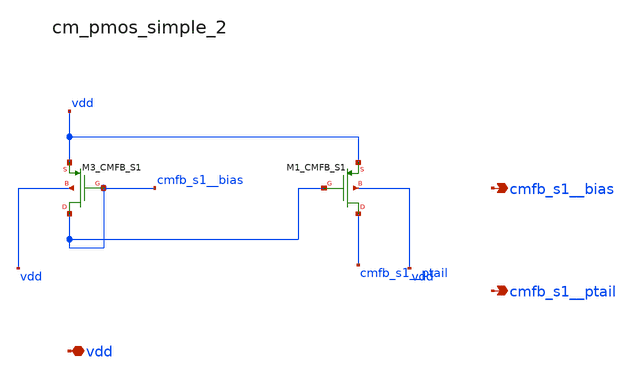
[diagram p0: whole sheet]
** sch_path: analog-db/raw/amp_035_fan_chopper_cmfb_dual/hier/blocks/cm_pmos_simple_2.sch
**.subckt cm_pmos_simple_2 vdd cmfb_s1__bias cmfb_s1__ptail
*.iopin vdd
*.opin cmfb_s1__bias
*.opin cmfb_s1__ptail
XM1_CMFB_S1 cmfb_s1__ptail cmfb_s1__bias vdd vdd sg13_lv_pmos w=x_dut_xm1_cmfb_s1_w
+ l=x_dut_xm1_cmfb_s1_l ng=1 m=x_dut_xm1_cmfb_s1_m
XM3_CMFB_S1 cmfb_s1__bias cmfb_s1__bias vdd vdd sg13_lv_pmos w=x_dut_xm3_cmfb_s1_w
+ l=x_dut_xm3_cmfb_s1_l ng=1 m=x_dut_xm3_cmfb_s1_m
**.ends
.end
